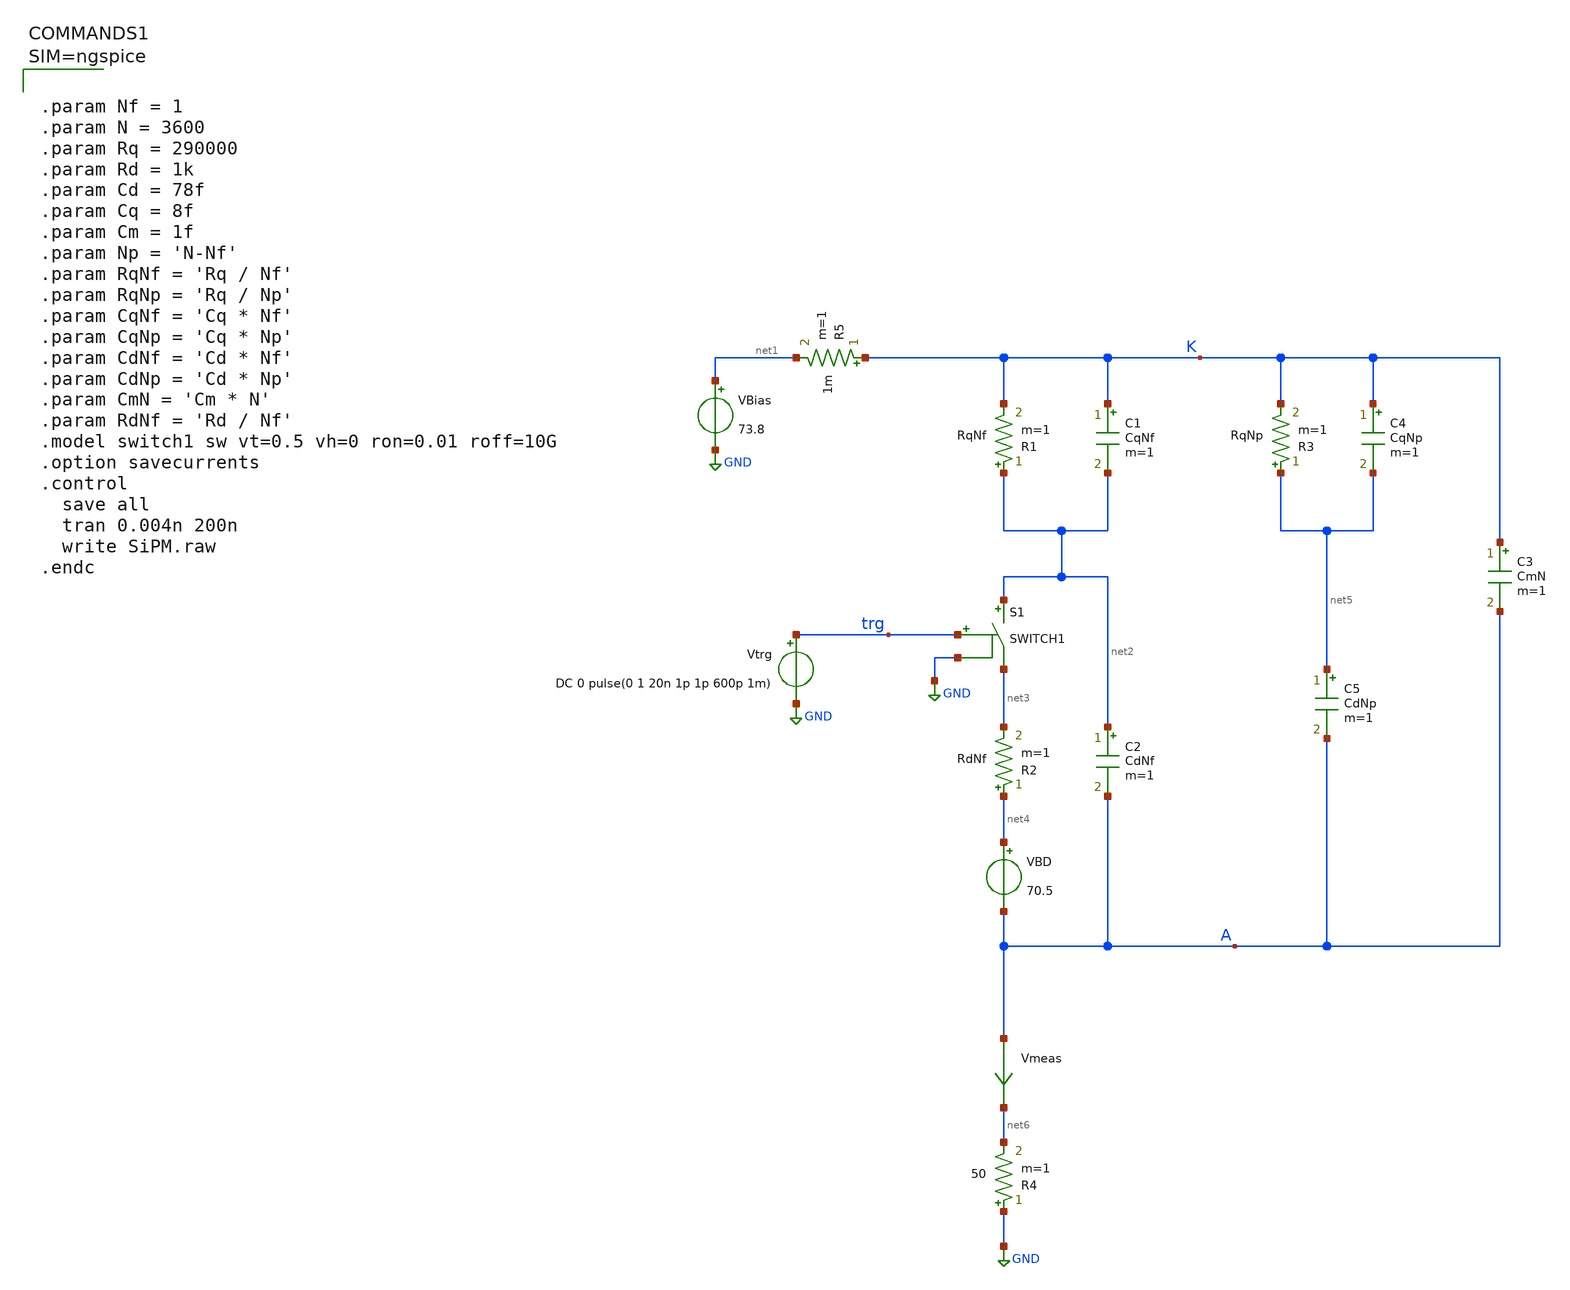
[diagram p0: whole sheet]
** sch_path: xschem/SiPM.sch
**.subckt SiPM
R5 K net1 1m m=1
R1 net2 K RqNf m=1
R2 net4 net3 RdNf m=1
VBD net4 A 70.5
C1 K net2 CqNf m=1
C2 net2 A CdNf m=1
R3 net5 K RqNp m=1
C3 K A CmN m=1
C4 K net5 CqNp m=1
C5 net5 A CdNp m=1
VBias net1 GND 73.8
Vtrg trg GND DC 0 pulse(0 1 20n 1p 1p 600p 1m)
R4 GND net6 50 m=1
S1 net2 net3 trg GND SWITCH1
Vmeas A net6 0
.save i(vmeas)
**** begin user architecture code



.param Nf = 1
.param N = 3600
.param Rq = 290000
.param Rd = 1k
.param Cd = 78f
.param Cq = 8f
.param Cm = 1f
.param Np = 'N-Nf'
.param RqNf = 'Rq / Nf'
.param RqNp = 'Rq / Np'
.param CqNf = 'Cq * Nf'
.param CqNp = 'Cq * Np'
.param CdNf = 'Cd * Nf'
.param CdNp = 'Cd * Np'
.param CmN = 'Cm * N'
.param RdNf = 'Rd / Nf'
.model switch1 sw vt=0.5 vh=0 ron=0.01 roff=10G
.option savecurrents
.control
  save all
  tran 0.004n 200n
  write SiPM.raw
.endc



**** end user architecture code
**.ends
.GLOBAL GND
.end
